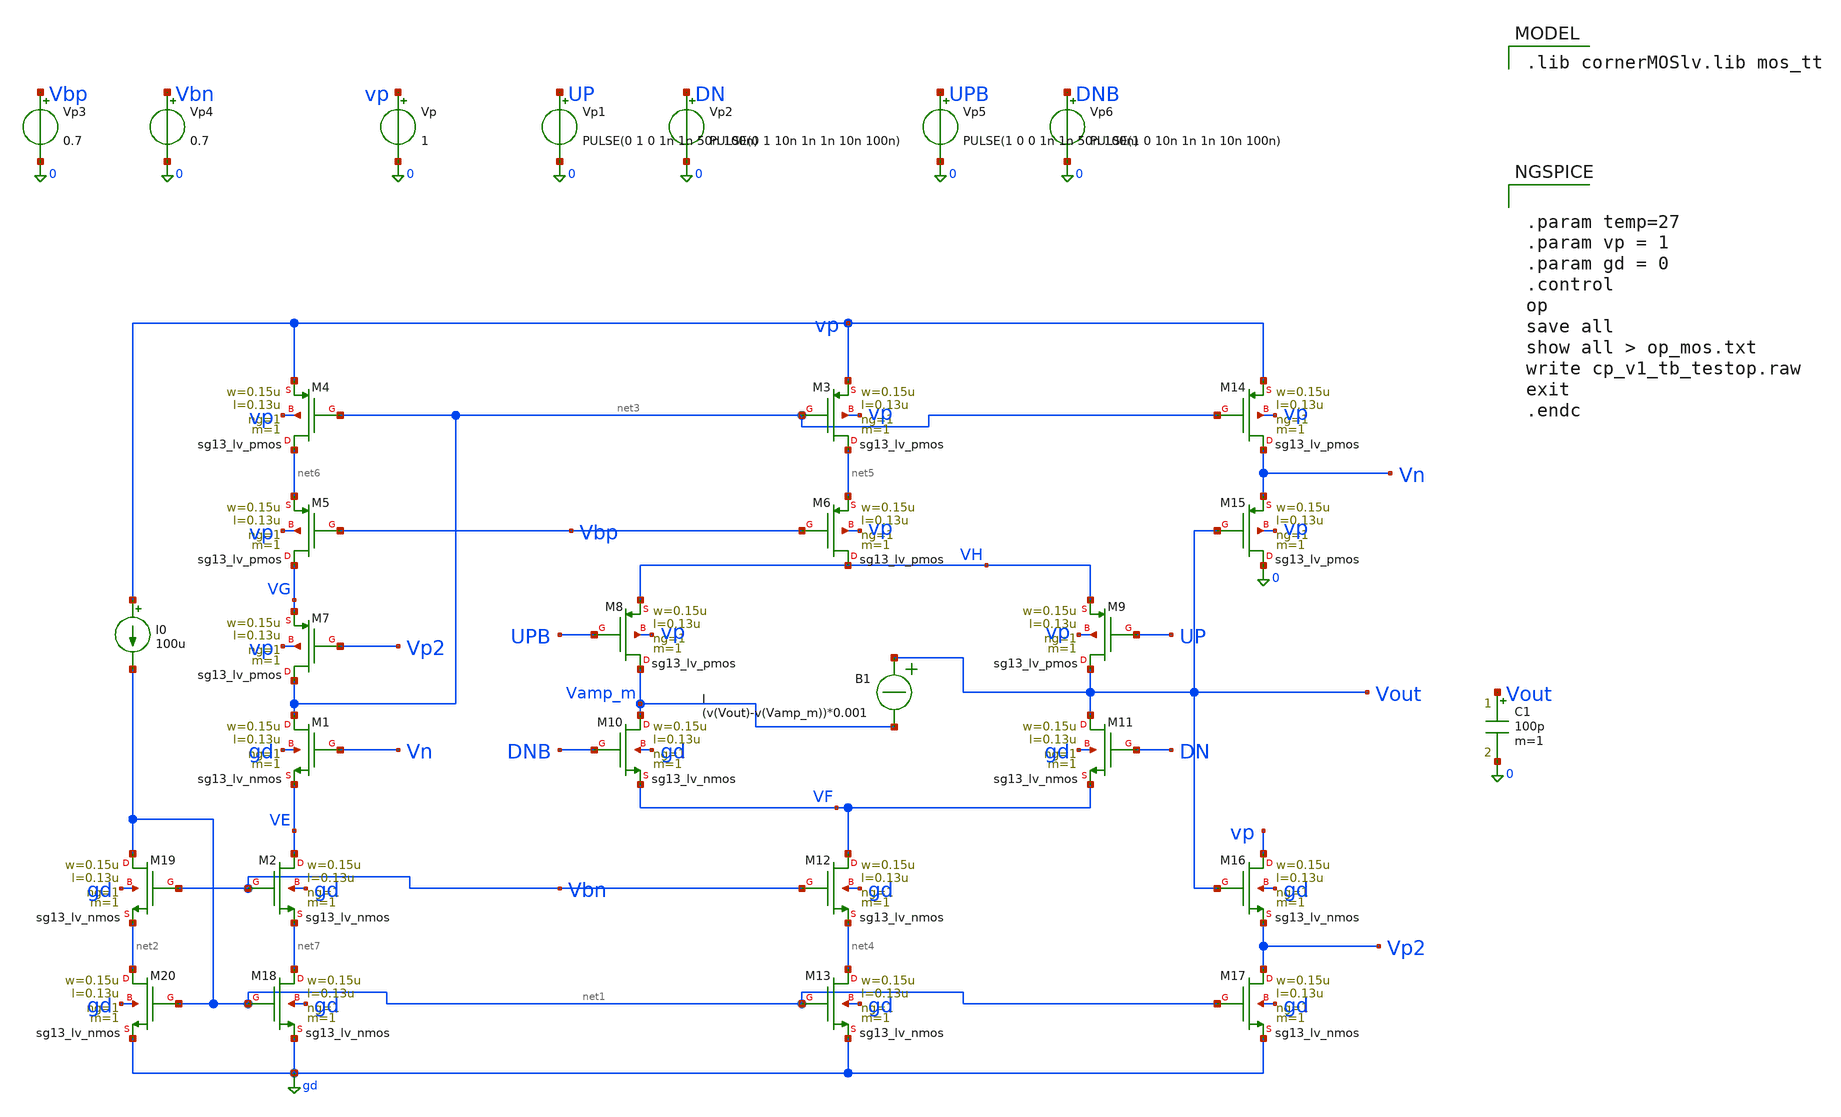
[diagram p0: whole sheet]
** sch_path: charge_pump/cp_v1_tb.sch
**.subckt cp_v1_tb
XM1 net3 Vn VE gd sg13_lv_nmos w=0.15u l=0.13u ng=1 m=1 mm_ok=1
XM3 net5 net3 vp vp sg13_lv_pmos w=0.15u l=0.13u ng=1 m=1 mm_ok=1
XM4 net6 net3 vp vp sg13_lv_pmos w=0.15u l=0.13u ng=1 m=1 mm_ok=1
XM5 VG Vbp net6 vp sg13_lv_pmos w=0.15u l=0.13u ng=1 m=1 mm_ok=1
XM6 VH Vbp net5 vp sg13_lv_pmos w=0.15u l=0.13u ng=1 m=1 mm_ok=1
XM7 net3 Vp2 VG vp sg13_lv_pmos w=0.15u l=0.13u ng=1 m=1 mm_ok=1
XM8 Vamp_m UPB VH vp sg13_lv_pmos w=0.15u l=0.13u ng=1 m=1 mm_ok=1
XM9 Vout UP VH vp sg13_lv_pmos w=0.15u l=0.13u ng=1 m=1 mm_ok=1
XM10 Vamp_m DNB VF gd sg13_lv_nmos w=0.15u l=0.13u ng=1 m=1 mm_ok=1
XM11 Vout DN VF gd sg13_lv_nmos w=0.15u l=0.13u ng=1 m=1 mm_ok=1
XM12 VF Vbn net4 gd sg13_lv_nmos w=0.15u l=0.13u ng=1 m=1 mm_ok=1
XM13 net4 net1 gd gd sg13_lv_nmos w=0.15u l=0.13u ng=1 m=1 mm_ok=1
XM14 Vn net3 vp vp sg13_lv_pmos w=0.15u l=0.13u ng=1 m=1 mm_ok=1
XM15 0 Vout Vn vp sg13_lv_pmos w=0.15u l=0.13u ng=1 m=1 mm_ok=1
XM16 vp Vout Vp2 gd sg13_lv_nmos w=0.15u l=0.13u ng=1 m=1 mm_ok=1
XM17 Vp2 net1 gd gd sg13_lv_nmos w=0.15u l=0.13u ng=1 m=1 mm_ok=1
XM2 VE Vbn net7 gd sg13_lv_nmos w=0.15u l=0.13u ng=1 m=1 mm_ok=1
XM18 net7 net1 gd gd sg13_lv_nmos w=0.15u l=0.13u ng=1 m=1 mm_ok=1
XM19 net1 Vbn net2 gd sg13_lv_nmos w=0.15u l=0.13u ng=1 m=1 mm_ok=1
XM20 net2 net1 gd gd sg13_lv_nmos w=0.15u l=0.13u ng=1 m=1 mm_ok=1
I0 vp net1 100u
B1 Vout Vamp_m I = (v(Vout)-v(Vamp_m))*0.001
C1 Vout 0 100p m=1
Vp vp 0 1
Vp1 UP 0 PULSE(0 1 0 1n 1n 50n 100n)
Vp2 DN 0 PULSE(0 1 10n 1n 1n 10n 100n)
Vp3 Vbp 0 0.7
Vp4 Vbn 0 0.7
Vp5 UPB 0 PULSE(1 0 0 1n 1n 50n 100n)
Vp6 DNB 0 PULSE(1 0 10n 1n 1n 10n 100n)
**** begin user architecture code
 .lib cornerMOSlv.lib mos_tt



.param temp=27
.param vp = 1
.param gd = 0
.control
op
save all
show all > op_mos.txt
write cp_v1_tb_testop.raw
exit
.endc


**** end user architecture code
**.ends
.GLOBAL gd
.end
